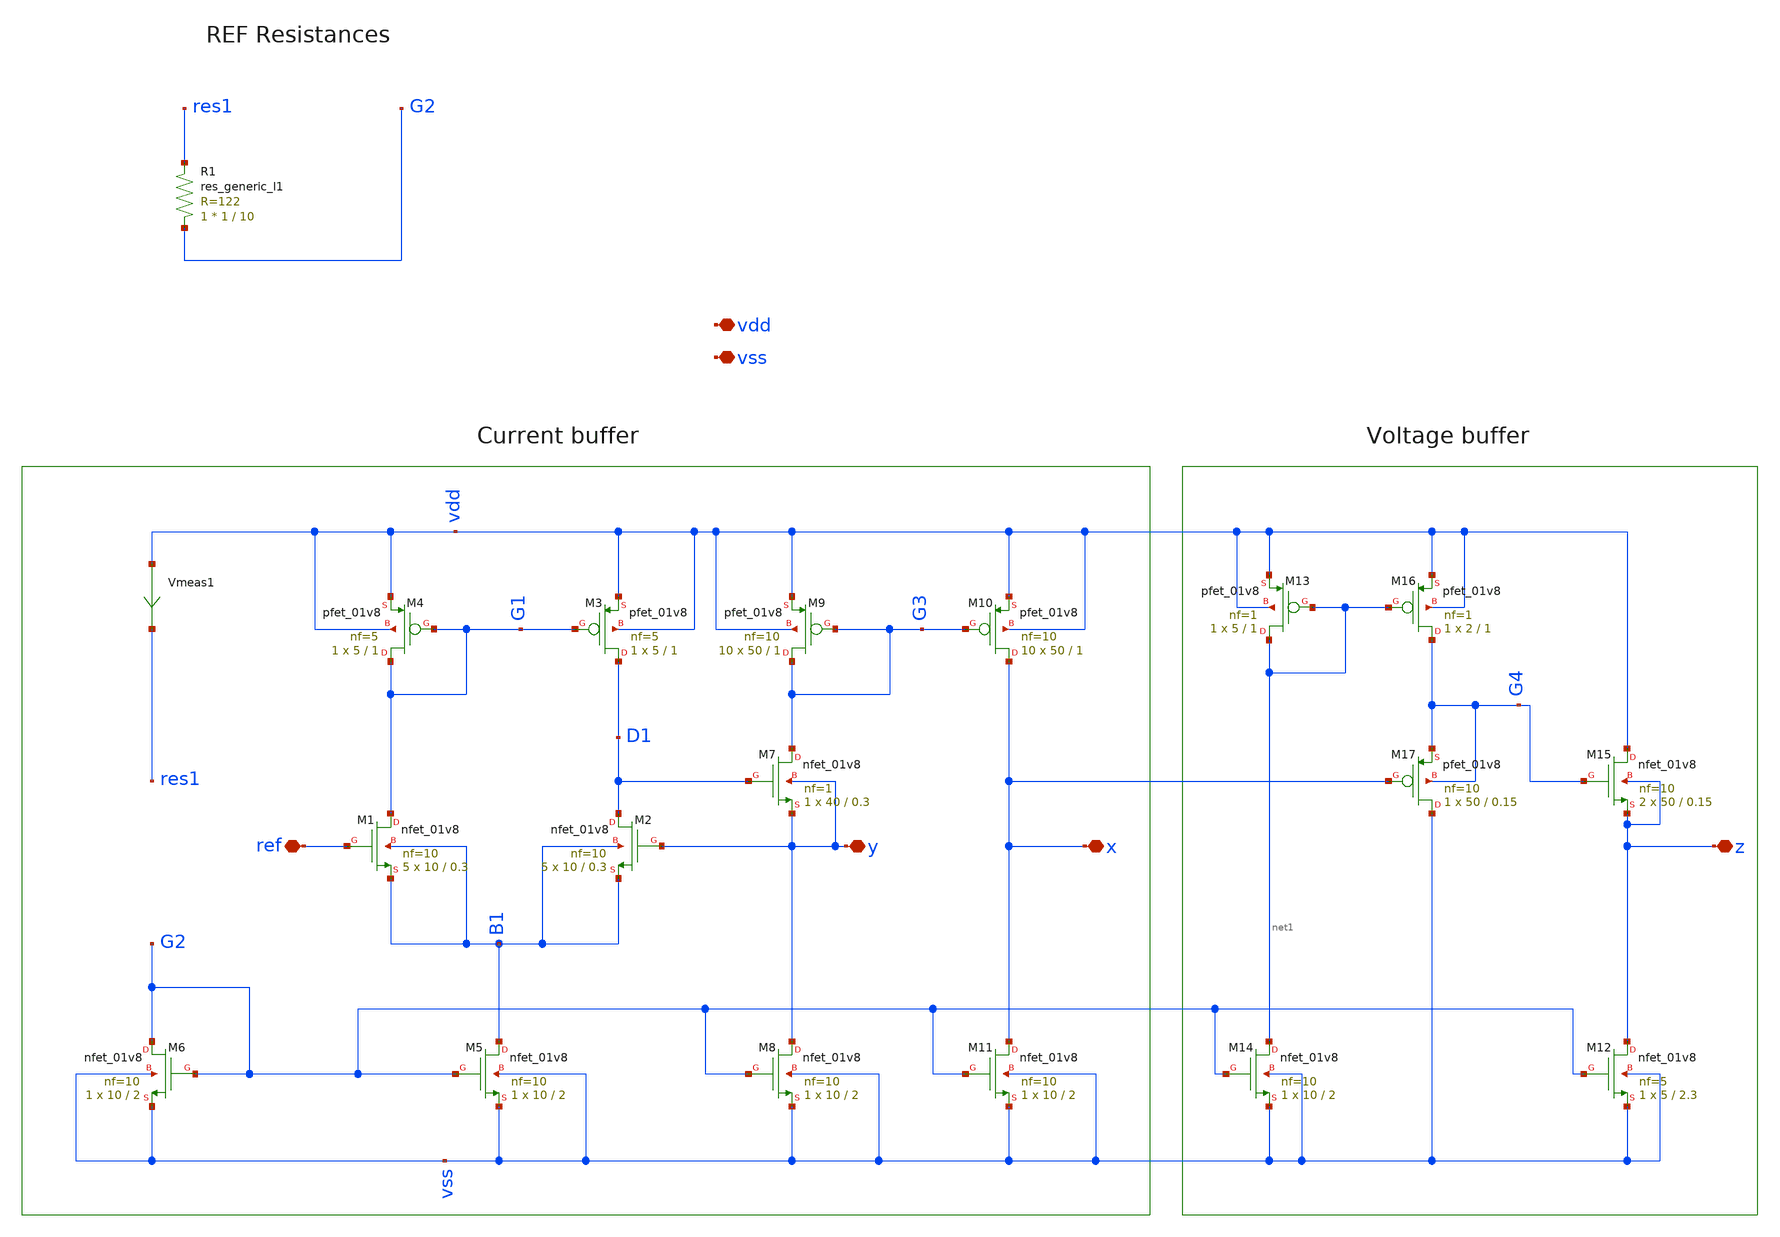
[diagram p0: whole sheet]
** sch_path: xschem/VCII-testRes.sch
**.subckt VCII-testRes x y z vdd vss ref
*.iopin x
*.iopin y
*.iopin z
*.iopin vdd
*.iopin vss
*.iopin ref
XM1 G1 ref B1 B1 sky130_fd_pr__nfet_01v8 L=0.3 W=10 nf=10 ad='int((nf+1)/2) * W/nf * 0.29' as='int((nf+2)/2) * W/nf * 0.29'
+ pd='2*int((nf+1)/2) * (W/nf + 0.29)' ps='2*int((nf+2)/2) * (W/nf + 0.29)' nrd='0.29 / W' nrs='0.29 / W'
+ sa=0 sb=0 sd=0 mult=5 m=5
XM2 D1 y B1 B1 sky130_fd_pr__nfet_01v8 L=0.3 W=10 nf=10 ad='int((nf+1)/2) * W/nf * 0.29' as='int((nf+2)/2) * W/nf * 0.29'
+ pd='2*int((nf+1)/2) * (W/nf + 0.29)' ps='2*int((nf+2)/2) * (W/nf + 0.29)' nrd='0.29 / W' nrs='0.29 / W'
+ sa=0 sb=0 sd=0 mult=5 m=5
XM3 D1 G1 vdd vdd sky130_fd_pr__pfet_01v8 L=1 W=5 nf=5 ad='int((nf+1)/2) * W/nf * 0.29' as='int((nf+2)/2) * W/nf * 0.29'
+ pd='2*int((nf+1)/2) * (W/nf + 0.29)' ps='2*int((nf+2)/2) * (W/nf + 0.29)' nrd='0.29 / W' nrs='0.29 / W'
+ sa=0 sb=0 sd=0 mult=1 m=1
XM4 G1 G1 vdd vdd sky130_fd_pr__pfet_01v8 L=1 W=5 nf=5 ad='int((nf+1)/2) * W/nf * 0.29' as='int((nf+2)/2) * W/nf * 0.29'
+ pd='2*int((nf+1)/2) * (W/nf + 0.29)' ps='2*int((nf+2)/2) * (W/nf + 0.29)' nrd='0.29 / W' nrs='0.29 / W'
+ sa=0 sb=0 sd=0 mult=1 m=1
XM5 B1 G2 vss vss sky130_fd_pr__nfet_01v8 L=2 W=10 nf=10 ad='int((nf+1)/2) * W/nf * 0.29' as='int((nf+2)/2) * W/nf * 0.29'
+ pd='2*int((nf+1)/2) * (W/nf + 0.29)' ps='2*int((nf+2)/2) * (W/nf + 0.29)' nrd='0.29 / W' nrs='0.29 / W'
+ sa=0 sb=0 sd=0 mult=1 m=1
XM6 G2 G2 vss vss sky130_fd_pr__nfet_01v8 L=2 W=10 nf=10 ad='int((nf+1)/2) * W/nf * 0.29' as='int((nf+2)/2) * W/nf * 0.29'
+ pd='2*int((nf+1)/2) * (W/nf + 0.29)' ps='2*int((nf+2)/2) * (W/nf + 0.29)' nrd='0.29 / W' nrs='0.29 / W'
+ sa=0 sb=0 sd=0 mult=1 m=1
XM7 G3 D1 y y sky130_fd_pr__nfet_01v8 L=0.3 W=40 nf=1 ad='int((nf+1)/2) * W/nf * 0.29' as='int((nf+2)/2) * W/nf * 0.29'
+ pd='2*int((nf+1)/2) * (W/nf + 0.29)' ps='2*int((nf+2)/2) * (W/nf + 0.29)' nrd='0.29 / W' nrs='0.29 / W'
+ sa=0 sb=0 sd=0 mult=1 m=1
XM8 y G2 vss vss sky130_fd_pr__nfet_01v8 L=2 W=10 nf=10 ad='int((nf+1)/2) * W/nf * 0.29' as='int((nf+2)/2) * W/nf * 0.29'
+ pd='2*int((nf+1)/2) * (W/nf + 0.29)' ps='2*int((nf+2)/2) * (W/nf + 0.29)' nrd='0.29 / W' nrs='0.29 / W'
+ sa=0 sb=0 sd=0 mult=1 m=1
XM9 G3 G3 vdd vdd sky130_fd_pr__pfet_01v8 L=1 W=50 nf=10 ad='int((nf+1)/2) * W/nf * 0.29' as='int((nf+2)/2) * W/nf * 0.29'
+ pd='2*int((nf+1)/2) * (W/nf + 0.29)' ps='2*int((nf+2)/2) * (W/nf + 0.29)' nrd='0.29 / W' nrs='0.29 / W'
+ sa=0 sb=0 sd=0 mult=10 m=10
XM10 x G3 vdd vdd sky130_fd_pr__pfet_01v8 L=1 W=50 nf=10 ad='int((nf+1)/2) * W/nf * 0.29' as='int((nf+2)/2) * W/nf * 0.29'
+ pd='2*int((nf+1)/2) * (W/nf + 0.29)' ps='2*int((nf+2)/2) * (W/nf + 0.29)' nrd='0.29 / W' nrs='0.29 / W'
+ sa=0 sb=0 sd=0 mult=10 m=10
XM11 x G2 vss vss sky130_fd_pr__nfet_01v8 L=2 W=10 nf=10 ad='int((nf+1)/2) * W/nf * 0.29' as='int((nf+2)/2) * W/nf * 0.29'
+ pd='2*int((nf+1)/2) * (W/nf + 0.29)' ps='2*int((nf+2)/2) * (W/nf + 0.29)' nrd='0.29 / W' nrs='0.29 / W'
+ sa=0 sb=0 sd=0 mult=1 m=1
XM14 net1 G2 vss vss sky130_fd_pr__nfet_01v8 L=2 W=10 nf=10 ad='int((nf+1)/2) * W/nf * 0.29' as='int((nf+2)/2) * W/nf * 0.29'
+ pd='2*int((nf+1)/2) * (W/nf + 0.29)' ps='2*int((nf+2)/2) * (W/nf + 0.29)' nrd='0.29 / W' nrs='0.29 / W'
+ sa=0 sb=0 sd=0 mult=1 m=1
XM12 z G2 vss vss sky130_fd_pr__nfet_01v8 L=2.3 W=5 nf=5 ad='int((nf+1)/2) * W/nf * 0.29' as='int((nf+2)/2) * W/nf * 0.29'
+ pd='2*int((nf+1)/2) * (W/nf + 0.29)' ps='2*int((nf+2)/2) * (W/nf + 0.29)' nrd='0.29 / W' nrs='0.29 / W'
+ sa=0 sb=0 sd=0 mult=1 m=1
XM15 vdd G4 z z sky130_fd_pr__nfet_01v8 L=0.15 W=50 nf=10 ad='int((nf+1)/2) * W/nf * 0.29' as='int((nf+2)/2) * W/nf * 0.29'
+ pd='2*int((nf+1)/2) * (W/nf + 0.29)' ps='2*int((nf+2)/2) * (W/nf + 0.29)' nrd='0.29 / W' nrs='0.29 / W'
+ sa=0 sb=0 sd=0 mult=2 m=2
XM13 net1 net1 vdd vdd sky130_fd_pr__pfet_01v8 L=1 W=5 nf=1 ad='int((nf+1)/2) * W/nf * 0.29' as='int((nf+2)/2) * W/nf * 0.29'
+ pd='2*int((nf+1)/2) * (W/nf + 0.29)' ps='2*int((nf+2)/2) * (W/nf + 0.29)' nrd='0.29 / W' nrs='0.29 / W'
+ sa=0 sb=0 sd=0 mult=1 m=1
XM16 G4 net1 vdd vdd sky130_fd_pr__pfet_01v8 L=1 W=2 nf=1 ad='int((nf+1)/2) * W/nf * 0.29' as='int((nf+2)/2) * W/nf * 0.29'
+ pd='2*int((nf+1)/2) * (W/nf + 0.29)' ps='2*int((nf+2)/2) * (W/nf + 0.29)' nrd='0.29 / W' nrs='0.29 / W'
+ sa=0 sb=0 sd=0 mult=1 m=1
XM17 vss x G4 G4 sky130_fd_pr__pfet_01v8 L=0.15 W=50 nf=10 ad='int((nf+1)/2) * W/nf * 0.29' as='int((nf+2)/2) * W/nf * 0.29'
+ pd='2*int((nf+1)/2) * (W/nf + 0.29)' ps='2*int((nf+2)/2) * (W/nf + 0.29)' nrd='0.29 / W' nrs='0.29 / W'
+ sa=0 sb=0 sd=0 mult=1 m=1
Vmeas1 vdd res1 0
.save i(vmeas1)
R1 G2 res1 sky130_fd_pr__res_generic_l1 W=1 L=10 m=1
**.ends
.end
